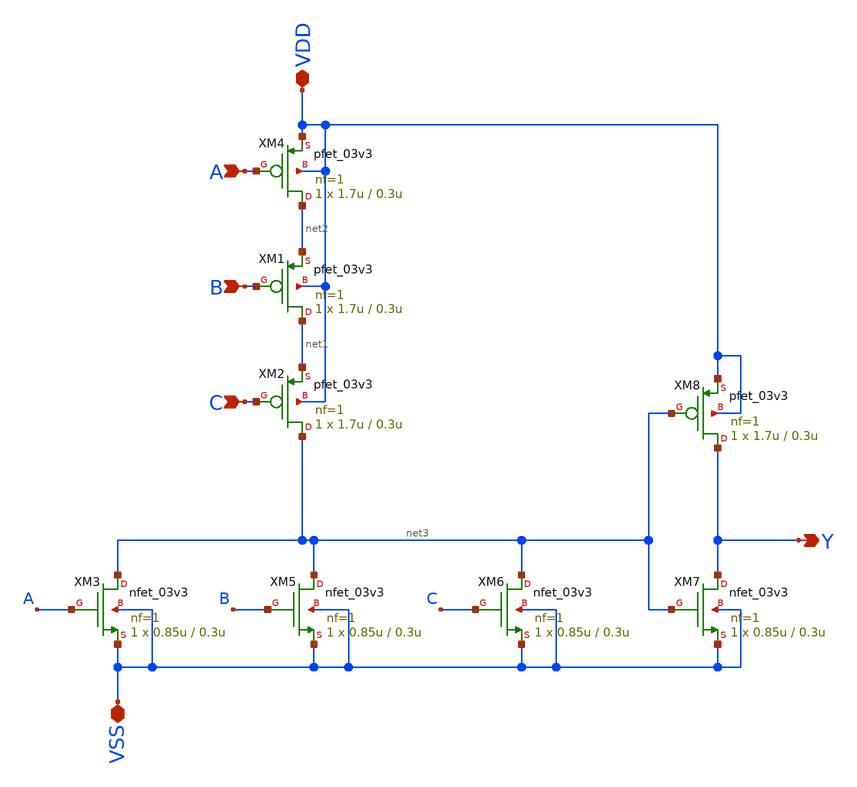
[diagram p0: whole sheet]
** sch_path: gf180mcu_osu_sc_gp9t3v3/xschem/gf180mcu_osu_sc_gp9t3v3__or3_1.sch
**.subckt gf180mcu_osu_sc_gp9t3v3__or3_1 A B C VDD Y VSS
*.ipin A
*.ipin B
*.ipin C
*.iopin VDD
*.opin Y
*.iopin VSS
XM4 net2 A VDD VDD pfet_03v3 L=0.3u W=1.7u nf=1 ad='int((nf+1)/2) * W/nf * 0.18u' as='int((nf+2)/2) * W/nf * 0.18u'
+ pd='2*int((nf+1)/2) * (W/nf + 0.18u)' ps='2*int((nf+2)/2) * (W/nf + 0.18u)' nrd='0.18u / W' nrs='0.18u / W'
+ sa=0 sb=0 sd=0 m=1
XM3 net3 A VSS VSS nfet_03v3 L=0.3u W=0.85u nf=1 ad='int((nf+1)/2) * W/nf * 0.18u' as='int((nf+2)/2) * W/nf * 0.18u'
+ pd='2*int((nf+1)/2) * (W/nf + 0.18u)' ps='2*int((nf+2)/2) * (W/nf + 0.18u)' nrd='0.18u / W' nrs='0.18u / W'
+ sa=0 sb=0 sd=0 m=1
XM1 net1 B net2 VDD pfet_03v3 L=0.3u W=1.7u nf=1 ad='int((nf+1)/2) * W/nf * 0.18u' as='int((nf+2)/2) * W/nf * 0.18u'
+ pd='2*int((nf+1)/2) * (W/nf + 0.18u)' ps='2*int((nf+2)/2) * (W/nf + 0.18u)' nrd='0.18u / W' nrs='0.18u / W'
+ sa=0 sb=0 sd=0 m=1
XM2 net3 C net1 VDD pfet_03v3 L=0.3u W=1.7u nf=1 ad='int((nf+1)/2) * W/nf * 0.18u' as='int((nf+2)/2) * W/nf * 0.18u'
+ pd='2*int((nf+1)/2) * (W/nf + 0.18u)' ps='2*int((nf+2)/2) * (W/nf + 0.18u)' nrd='0.18u / W' nrs='0.18u / W'
+ sa=0 sb=0 sd=0 m=1
XM5 net3 B VSS VSS nfet_03v3 L=0.3u W=0.85u nf=1 ad='int((nf+1)/2) * W/nf * 0.18u' as='int((nf+2)/2) * W/nf * 0.18u'
+ pd='2*int((nf+1)/2) * (W/nf + 0.18u)' ps='2*int((nf+2)/2) * (W/nf + 0.18u)' nrd='0.18u / W' nrs='0.18u / W'
+ sa=0 sb=0 sd=0 m=1
XM6 net3 C VSS VSS nfet_03v3 L=0.3u W=0.85u nf=1 ad='int((nf+1)/2) * W/nf * 0.18u' as='int((nf+2)/2) * W/nf * 0.18u'
+ pd='2*int((nf+1)/2) * (W/nf + 0.18u)' ps='2*int((nf+2)/2) * (W/nf + 0.18u)' nrd='0.18u / W' nrs='0.18u / W'
+ sa=0 sb=0 sd=0 m=1
XM7 Y net3 VSS VSS nfet_03v3 L=0.3u W=0.85u nf=1 ad='int((nf+1)/2) * W/nf * 0.18u' as='int((nf+2)/2) * W/nf * 0.18u'
+ pd='2*int((nf+1)/2) * (W/nf + 0.18u)' ps='2*int((nf+2)/2) * (W/nf + 0.18u)' nrd='0.18u / W' nrs='0.18u / W'
+ sa=0 sb=0 sd=0 m=1
XM8 Y net3 VDD VDD pfet_03v3 L=0.3u W=1.7u nf=1 ad='int((nf+1)/2) * W/nf * 0.18u' as='int((nf+2)/2) * W/nf * 0.18u'
+ pd='2*int((nf+1)/2) * (W/nf + 0.18u)' ps='2*int((nf+2)/2) * (W/nf + 0.18u)' nrd='0.18u / W' nrs='0.18u / W'
+ sa=0 sb=0 sd=0 m=1
**.ends
.end
